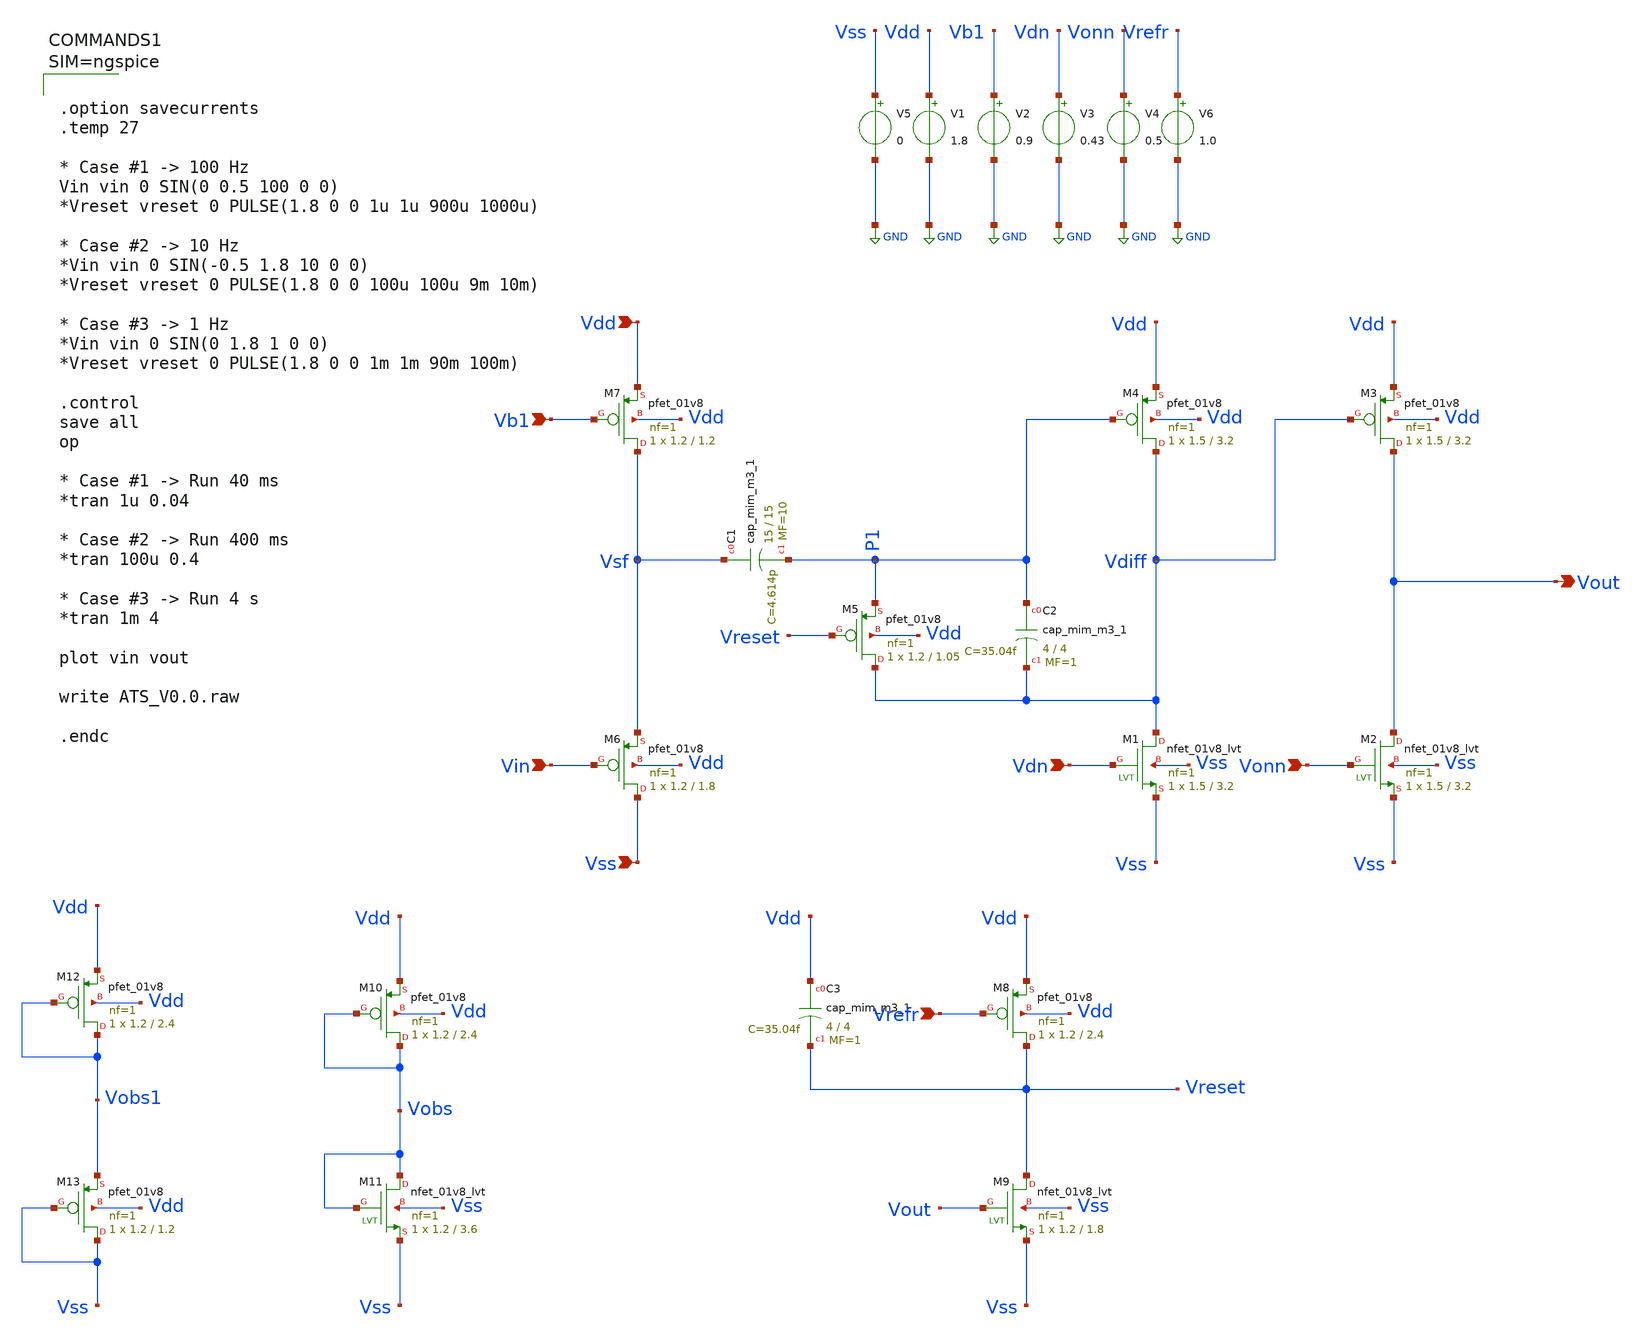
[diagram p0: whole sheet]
** sch_path: testbenches/ATS_V0.0_tb.sch
**.subckt ATS_V0.0_tb Vdd Vss Vdn Vonn Vb1 Vin Vout Vrefr
*.ipin Vdd
*.ipin Vss
*.ipin Vdn
*.ipin Vonn
*.ipin Vb1
*.ipin Vin
*.opin Vout
*.ipin Vrefr
XM3 Vout Vdiff Vdd Vdd sky130_fd_pr__pfet_01v8 L=3.2 W=1.5 nf=1 ad='int((nf+1)/2) * W/nf * 0.29' as='int((nf+2)/2) * W/nf * 0.29'
+ pd='2*int((nf+1)/2) * (W/nf + 0.29)' ps='2*int((nf+2)/2) * (W/nf + 0.29)' nrd='0.29 / W' nrs='0.29 / W'
+ sa=0 sb=0 sd=0 mult=1 m=1
XM4 Vdiff P1 Vdd Vdd sky130_fd_pr__pfet_01v8 L=3.2 W=1.5 nf=1 ad='int((nf+1)/2) * W/nf * 0.29' as='int((nf+2)/2) * W/nf * 0.29'
+ pd='2*int((nf+1)/2) * (W/nf + 0.29)' ps='2*int((nf+2)/2) * (W/nf + 0.29)' nrd='0.29 / W' nrs='0.29 / W'
+ sa=0 sb=0 sd=0 mult=1 m=1
XM5 Vdiff Vreset P1 Vdd sky130_fd_pr__pfet_01v8 L=1.05 W=1.2 nf=1 ad='int((nf+1)/2) * W/nf * 0.29' as='int((nf+2)/2) * W/nf * 0.29'
+ pd='2*int((nf+1)/2) * (W/nf + 0.29)' ps='2*int((nf+2)/2) * (W/nf + 0.29)' nrd='0.29 / W' nrs='0.29 / W'
+ sa=0 sb=0 sd=0 mult=1 m=1
XM6 Vss Vin Vsf Vdd sky130_fd_pr__pfet_01v8 L=1.8 W=1.2 nf=1 ad='int((nf+1)/2) * W/nf * 0.29' as='int((nf+2)/2) * W/nf * 0.29'
+ pd='2*int((nf+1)/2) * (W/nf + 0.29)' ps='2*int((nf+2)/2) * (W/nf + 0.29)' nrd='0.29 / W' nrs='0.29 / W'
+ sa=0 sb=0 sd=0 mult=1 m=1
XM7 Vsf Vb1 Vdd Vdd sky130_fd_pr__pfet_01v8 L=1.2 W=1.2 nf=1 ad='int((nf+1)/2) * W/nf * 0.29' as='int((nf+2)/2) * W/nf * 0.29'
+ pd='2*int((nf+1)/2) * (W/nf + 0.29)' ps='2*int((nf+2)/2) * (W/nf + 0.29)' nrd='0.29 / W' nrs='0.29 / W'
+ sa=0 sb=0 sd=0 mult=1 m=1
XC1 Vsf P1 sky130_fd_pr__cap_mim_m3_1 W=15 L=15 MF=10 m=10
XC2 P1 Vdiff sky130_fd_pr__cap_mim_m3_1 W=4 L=4 MF=1 m=1
V1 Vdd GND 1.8
V2 Vb1 GND 0.9
V3 Vdn GND 0.43
V4 Vonn GND 0.5
V5 Vss GND 0
XM1 Vdiff Vdn Vss Vss sky130_fd_pr__nfet_01v8_lvt L=3.2 W=1.5 nf=1 ad='int((nf+1)/2) * W/nf * 0.29' as='int((nf+2)/2) * W/nf * 0.29'
+ pd='2*int((nf+1)/2) * (W/nf + 0.29)' ps='2*int((nf+2)/2) * (W/nf + 0.29)' nrd='0.29 / W' nrs='0.29 / W'
+ sa=0 sb=0 sd=0 mult=1 m=1
XM2 Vout Vonn Vss Vss sky130_fd_pr__nfet_01v8_lvt L=3.2 W=1.5 nf=1 ad='int((nf+1)/2) * W/nf * 0.29' as='int((nf+2)/2) * W/nf * 0.29'
+ pd='2*int((nf+1)/2) * (W/nf + 0.29)' ps='2*int((nf+2)/2) * (W/nf + 0.29)' nrd='0.29 / W' nrs='0.29 / W'
+ sa=0 sb=0 sd=0 mult=1 m=1
XM8 Vreset Vrefr Vdd Vdd sky130_fd_pr__pfet_01v8 L=2.4 W=1.2 nf=1 ad='int((nf+1)/2) * W/nf * 0.29' as='int((nf+2)/2) * W/nf * 0.29'
+ pd='2*int((nf+1)/2) * (W/nf + 0.29)' ps='2*int((nf+2)/2) * (W/nf + 0.29)' nrd='0.29 / W' nrs='0.29 / W'
+ sa=0 sb=0 sd=0 mult=1 m=1
XM9 Vreset Vout Vss Vss sky130_fd_pr__nfet_01v8_lvt L=1.8 W=1.2 nf=1 ad='int((nf+1)/2) * W/nf * 0.29'
+ as='int((nf+2)/2) * W/nf * 0.29' pd='2*int((nf+1)/2) * (W/nf + 0.29)' ps='2*int((nf+2)/2) * (W/nf + 0.29)'
+ nrd='0.29 / W' nrs='0.29 / W' sa=0 sb=0 sd=0 mult=1 m=1
XC3 Vdd Vreset sky130_fd_pr__cap_mim_m3_1 W=4 L=4 MF=1 m=1
V6 Vrefr GND 1.0
XM10 Vobs Vobs Vdd Vdd sky130_fd_pr__pfet_01v8 L=2.4 W=1.2 nf=1 ad='int((nf+1)/2) * W/nf * 0.29' as='int((nf+2)/2) * W/nf * 0.29'
+ pd='2*int((nf+1)/2) * (W/nf + 0.29)' ps='2*int((nf+2)/2) * (W/nf + 0.29)' nrd='0.29 / W' nrs='0.29 / W'
+ sa=0 sb=0 sd=0 mult=1 m=1
XM11 Vobs Vobs Vss Vss sky130_fd_pr__nfet_01v8_lvt L=3.6 W=1.2 nf=1 ad='int((nf+1)/2) * W/nf * 0.29'
+ as='int((nf+2)/2) * W/nf * 0.29' pd='2*int((nf+1)/2) * (W/nf + 0.29)' ps='2*int((nf+2)/2) * (W/nf + 0.29)'
+ nrd='0.29 / W' nrs='0.29 / W' sa=0 sb=0 sd=0 mult=1 m=1
XM12 Vobs1 Vobs1 Vdd Vdd sky130_fd_pr__pfet_01v8 L=2.4 W=1.2 nf=1 ad='int((nf+1)/2) * W/nf * 0.29' as='int((nf+2)/2) * W/nf * 0.29'
+ pd='2*int((nf+1)/2) * (W/nf + 0.29)' ps='2*int((nf+2)/2) * (W/nf + 0.29)' nrd='0.29 / W' nrs='0.29 / W'
+ sa=0 sb=0 sd=0 mult=1 m=1
XM13 Vss Vss Vobs1 Vdd sky130_fd_pr__pfet_01v8 L=1.2 W=1.2 nf=1 ad='int((nf+1)/2) * W/nf * 0.29' as='int((nf+2)/2) * W/nf * 0.29'
+ pd='2*int((nf+1)/2) * (W/nf + 0.29)' ps='2*int((nf+2)/2) * (W/nf + 0.29)' nrd='0.29 / W' nrs='0.29 / W'
+ sa=0 sb=0 sd=0 mult=1 m=1
**** begin user architecture code

** opencircuitdesign pdks install
.lib $::SKYWATER_MODELS/sky130.lib.spice tt





.option savecurrents
.temp 27

* Case #1 -> 100 Hz
Vin vin 0 SIN(0 0.5 100 0 0)
*Vreset vreset 0 PULSE(1.8 0 0 1u 1u 900u 1000u)

* Case #2 -> 10 Hz
*Vin vin 0 SIN(-0.5 1.8 10 0 0)
*Vreset vreset 0 PULSE(1.8 0 0 100u 100u 9m 10m)

* Case #3 -> 1 Hz
*Vin vin 0 SIN(0 1.8 1 0 0)
*Vreset vreset 0 PULSE(1.8 0 0 1m 1m 90m 100m)

.control
save all
op

* Case #1 -> Run 40 ms
*tran 1u 0.04

* Case #2 -> Run 400 ms
*tran 100u 0.4

* Case #3 -> Run 4 s
*tran 1m 4

plot vin vout

write ATS_V0.0.raw

.endc



**** end user architecture code
**.ends
.GLOBAL GND
.end
